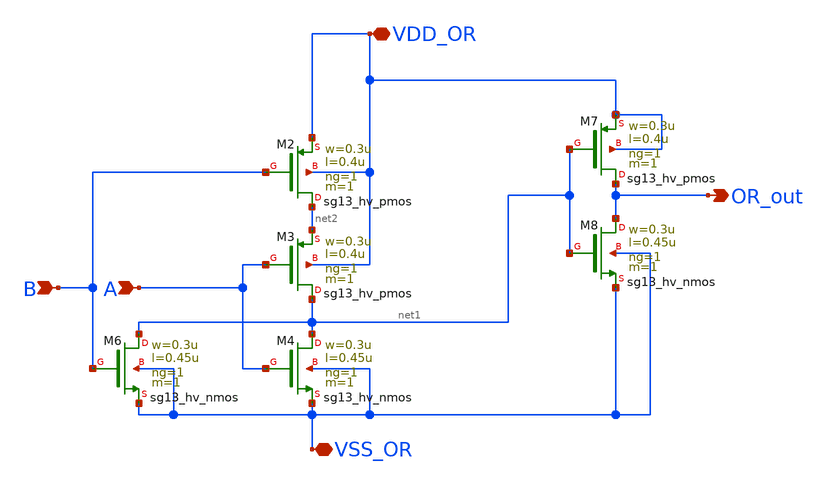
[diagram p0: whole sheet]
** sch_path: circuit_files/xschem_symbols/simp_OR.sch
**.subckt simp_OR VDD_OR VSS_OR OR_out B A
*.iopin VDD_OR
*.iopin VSS_OR
*.opin OR_out
*.ipin B
*.ipin A
XM2 net2 B VDD_OR VDD_OR sg13_hv_pmos w=0.3u l=0.4u ng=1 m=1 mm_ok=1
XM3 net1 A net2 VDD_OR sg13_hv_pmos w=0.3u l=0.4u ng=1 m=1 mm_ok=1
XM4 net1 A VSS_OR VSS_OR sg13_hv_nmos w=0.3u l=0.45u ng=1 m=1 mm_ok=1
XM6 net1 B VSS_OR VSS_OR sg13_hv_nmos w=0.3u l=0.45u ng=1 m=1 mm_ok=1
XM7 OR_out net1 VDD_OR VDD_OR sg13_hv_pmos w=0.3u l=0.4u ng=1 m=1 mm_ok=1
XM8 OR_out net1 VSS_OR VSS_OR sg13_hv_nmos w=0.3u l=0.45u ng=1 m=1 mm_ok=1
**.ends
.end
